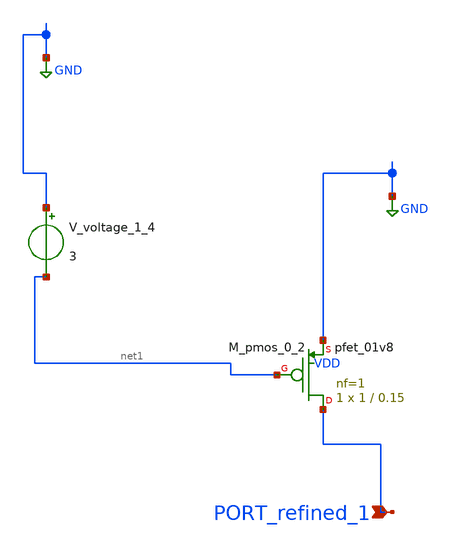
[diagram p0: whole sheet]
** sch_path: schematics/AMSNet/1.sch
**.subckt 1 PORT_refined_1
*.ipin PORT_refined_1
XM_pmos_0_2 PORT_refined_1 net1 GND VDD sky130_fd_pr__pfet_01v8 L=0.15 W=1 nf=1 ad='int((1 + 1)/2) * 1 / 1 * 0.29'
+ as='int((1 + 2)/2) * 1 / 1 * 0.29' pd='2*int((1 + 1)/2) * (1 / 1 + 0.29)' ps='2*int((1 + 2)/2) * (1 / 1 + 0.29)'
+ nrd='0.29 / 1 ' nrs='0.29 / 1 ' sa=0 sb=0 sd=0 mult=1 m=1
V_voltage_1_4 GND net1 3
**.ends
.GLOBAL GND
.end
